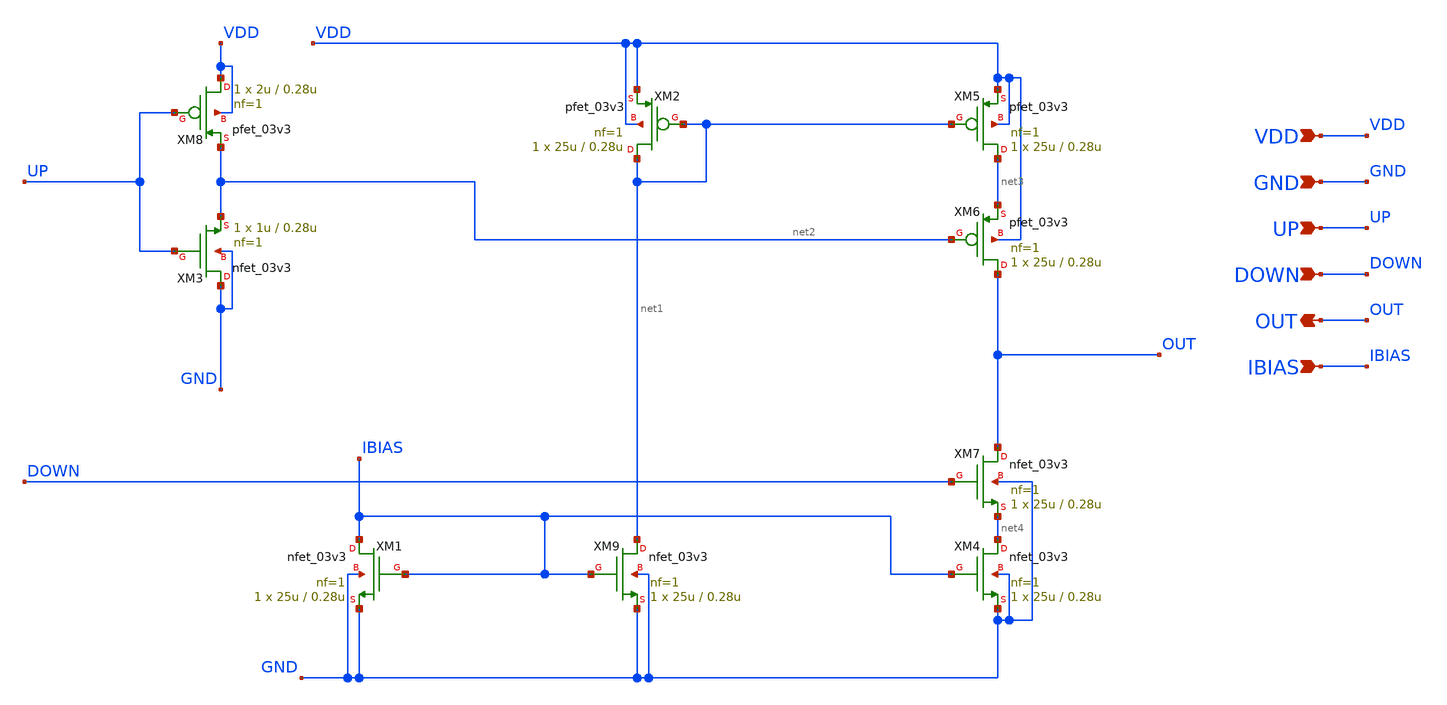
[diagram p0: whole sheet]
** sch_path: designs/libs/core_analog/charge_pump/charge_pump.sch
**.subckt charge_pump VDD GND OUT IBIAS UP DOWN
*.ipin VDD
*.ipin GND
*.opin OUT
*.ipin IBIAS
*.ipin UP
*.ipin DOWN
XM1 IBIAS IBIAS GND GND nfet_03v3 L=0.28u W=25u nf=1 ad='int((nf+1)/2) * W/nf * 0.18u' as='int((nf+2)/2) * W/nf * 0.18u'
+ pd='2*int((nf+1)/2) * (W/nf + 0.18u)' ps='2*int((nf+2)/2) * (W/nf + 0.18u)' nrd='0.18u / W' nrs='0.18u / W'
+ sa=0 sb=0 sd=0 m=1
XM2 net1 net1 VDD VDD pfet_03v3 L=0.28u W=25u nf=1 ad='int((nf+1)/2) * W/nf * 0.18u' as='int((nf+2)/2) * W/nf * 0.18u'
+ pd='2*int((nf+1)/2) * (W/nf + 0.18u)' ps='2*int((nf+2)/2) * (W/nf + 0.18u)' nrd='0.18u / W' nrs='0.18u / W'
+ sa=0 sb=0 sd=0 m=1
XM4 net4 IBIAS GND GND nfet_03v3 L=0.28u W=25u nf=1 ad='int((nf+1)/2) * W/nf * 0.18u' as='int((nf+2)/2) * W/nf * 0.18u'
+ pd='2*int((nf+1)/2) * (W/nf + 0.18u)' ps='2*int((nf+2)/2) * (W/nf + 0.18u)' nrd='0.18u / W' nrs='0.18u / W'
+ sa=0 sb=0 sd=0 m=1
XM5 net3 net1 VDD VDD pfet_03v3 L=0.28u W=25u nf=1 ad='int((nf+1)/2) * W/nf * 0.18u' as='int((nf+2)/2) * W/nf * 0.18u'
+ pd='2*int((nf+1)/2) * (W/nf + 0.18u)' ps='2*int((nf+2)/2) * (W/nf + 0.18u)' nrd='0.18u / W' nrs='0.18u / W'
+ sa=0 sb=0 sd=0 m=1
XM6 OUT net2 net3 VDD pfet_03v3 L=0.28u W=25u nf=1 ad='int((nf+1)/2) * W/nf * 0.18u' as='int((nf+2)/2) * W/nf * 0.18u'
+ pd='2*int((nf+1)/2) * (W/nf + 0.18u)' ps='2*int((nf+2)/2) * (W/nf + 0.18u)' nrd='0.18u / W' nrs='0.18u / W'
+ sa=0 sb=0 sd=0 m=1
XM7 OUT DOWN net4 GND nfet_03v3 L=0.28u W=25u nf=1 ad='int((nf+1)/2) * W/nf * 0.18u' as='int((nf+2)/2) * W/nf * 0.18u'
+ pd='2*int((nf+1)/2) * (W/nf + 0.18u)' ps='2*int((nf+2)/2) * (W/nf + 0.18u)' nrd='0.18u / W' nrs='0.18u / W'
+ sa=0 sb=0 sd=0 m=1
XM9 net1 IBIAS GND GND nfet_03v3 L=0.28u W=25u nf=1 ad='int((nf+1)/2) * W/nf * 0.18u' as='int((nf+2)/2) * W/nf * 0.18u'
+ pd='2*int((nf+1)/2) * (W/nf + 0.18u)' ps='2*int((nf+2)/2) * (W/nf + 0.18u)' nrd='0.18u / W' nrs='0.18u / W'
+ sa=0 sb=0 sd=0 m=1
XM3 GND UP net2 GND nfet_03v3 L=0.28u W=1u nf=1 ad='int((nf+1)/2) * W/nf * 0.18u' as='int((nf+2)/2) * W/nf * 0.18u'
+ pd='2*int((nf+1)/2) * (W/nf + 0.18u)' ps='2*int((nf+2)/2) * (W/nf + 0.18u)' nrd='0.18u / W' nrs='0.18u / W'
+ sa=0 sb=0 sd=0 m=1
XM8 VDD UP net2 VDD pfet_03v3 L=0.28u W=2u nf=1 ad='int((nf+1)/2) * W/nf * 0.18u' as='int((nf+2)/2) * W/nf * 0.18u'
+ pd='2*int((nf+1)/2) * (W/nf + 0.18u)' ps='2*int((nf+2)/2) * (W/nf + 0.18u)' nrd='0.18u / W' nrs='0.18u / W'
+ sa=0 sb=0 sd=0 m=1
**.ends
.end
